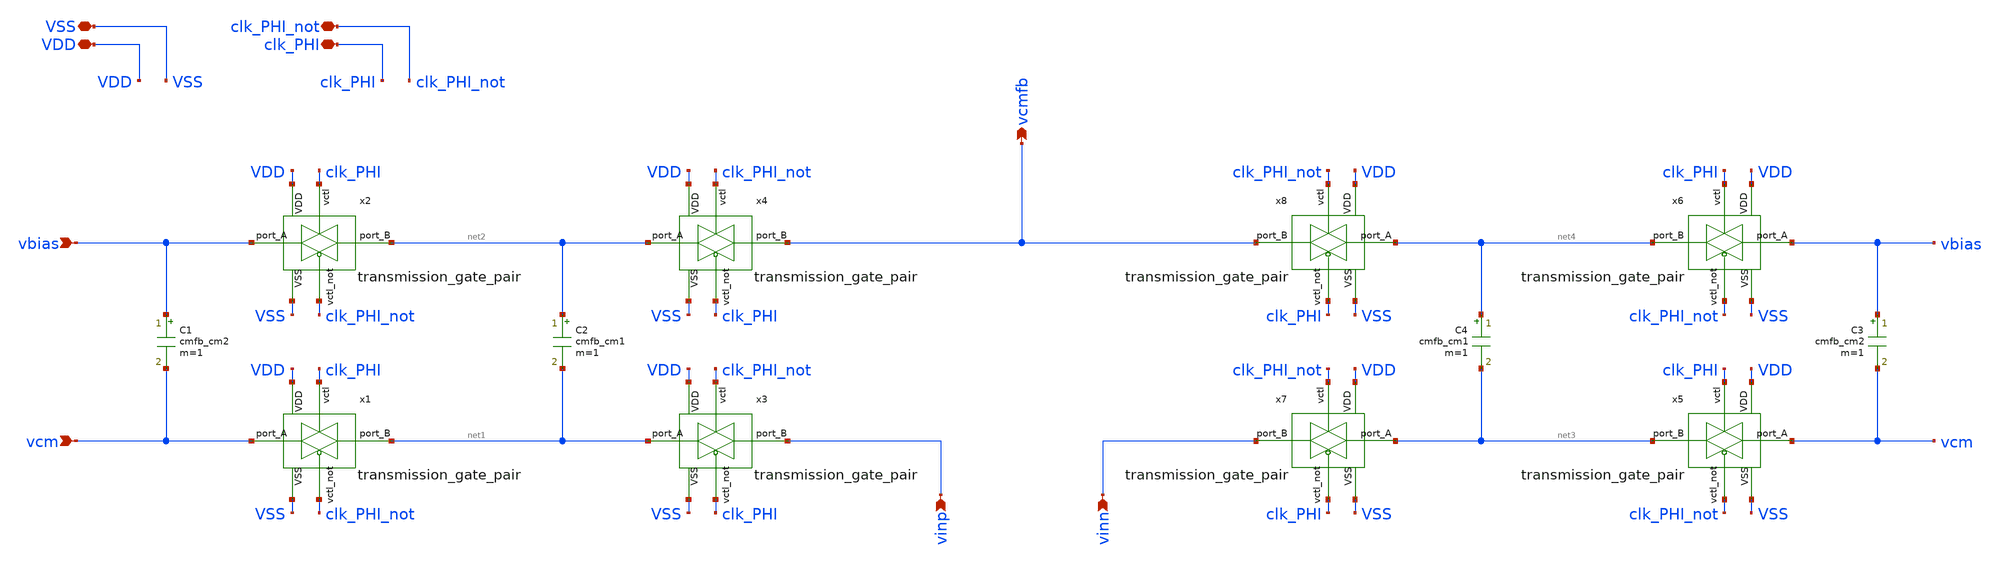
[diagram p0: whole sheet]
** sch_path: analog-db/drawings/shared/cmfb-output-switched-cap.sch
* Copyright 2026 MacAnalog Research Group
**.subckt cmfb-output-switched-cap VSS VDD vinp vinn vcmfb vbias clk_PHI_not clk_PHI vcm
*.iopin VSS
*.iopin VDD
*.ipin vinp
*.ipin vinn
*.opin vcmfb
*.ipin vbias
*.iopin clk_PHI_not
*.iopin clk_PHI
*.ipin vcm
C1 vbias vcm cmfb_cm2 m=1
C2 net2 net1 cmfb_cm1 m=1
x1 clk_PHI_not VDD net1 VSS vcm clk_PHI transmission_gate_pair
x2 clk_PHI_not VDD net2 VSS vbias clk_PHI transmission_gate_pair
x3 clk_PHI VDD vinp VSS net1 clk_PHI_not transmission_gate_pair
x4 clk_PHI VDD vcmfb VSS net2 clk_PHI_not transmission_gate_pair
C3 vbias vcm cmfb_cm2 m=1
C4 net4 net3 cmfb_cm1 m=1
x5 clk_PHI_not VDD net3 VSS vcm clk_PHI transmission_gate_pair
x6 clk_PHI_not VDD net4 VSS vbias clk_PHI transmission_gate_pair
x7 clk_PHI VDD vinn VSS net3 clk_PHI_not transmission_gate_pair
x8 clk_PHI VDD vcmfb VSS net4 clk_PHI_not transmission_gate_pair
**.ends

* expanding   symbol:  shared/transmission_gate_pair.sym # of pins=6
** sym_path: analog-db/drawings/shared/transmission_gate_pair.sym
** sch_path: analog-db/drawings/shared/transmission_gate_pair.sch
.subckt transmission_gate_pair vctl_not VDD port_B VSS port_A vctl
*.ipin port_A
*.ipin port_B
*.ipin vctl
*.ipin VSS
*.ipin VDD
*.ipin vctl_not
XM1 port_A vctl port_B VSS sg13_lv_nmos w=tg_n_w l=tg_n_l ng=1 m=1 mm_ok=1
XM2 port_B vctl_not port_A VDD sg13_lv_pmos w=tg_p_w l=tg_p_l ng=1 m=1 mm_ok=1
.ends

.end
